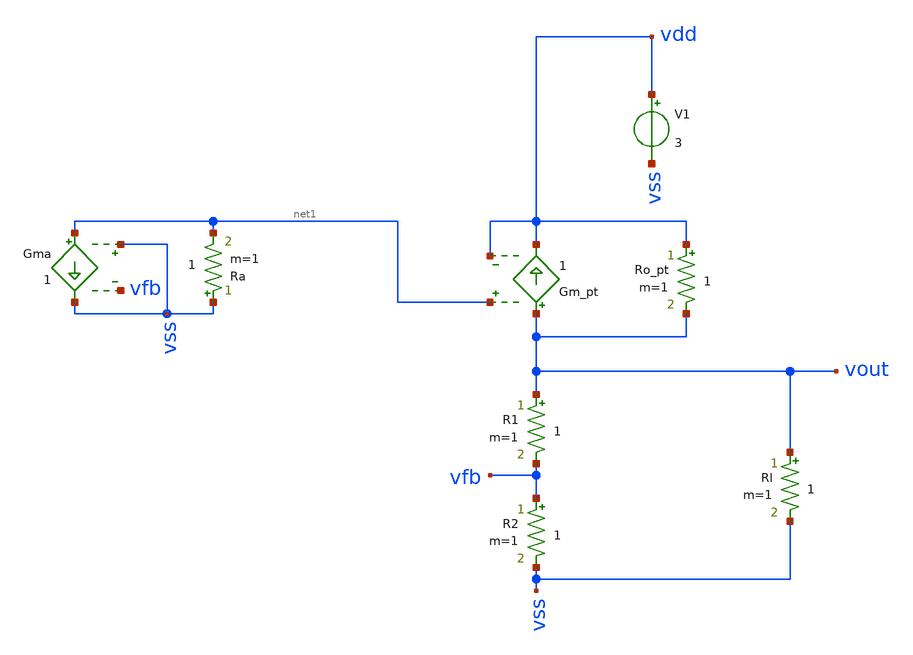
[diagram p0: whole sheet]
** sch_path: test/Tesis_notebooks/xschem/ldo_psrr.sch
**.subckt ldo_psrr
Ro_pt vdd vout 1 m=1
Gm_pt vout vdd net1 vdd 1
R1 vout vfb 1 m=1
R2 vfb vss 1 m=1
Gma net1 vss vss vfb 1
Ra vss net1 1 m=1
V1 vdd vss 3
Rl vout vss 1 m=1
**.ends
.end
